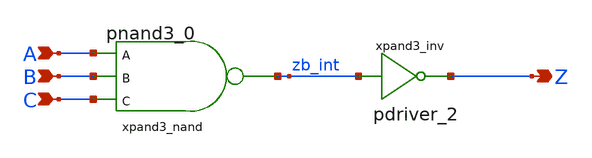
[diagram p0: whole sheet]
** sch_path: sram_2_16_scn4m/pand3.sch
**.subckt pand3 A B C Z
*.ipin A
*.ipin B
*.ipin C
*.opin Z
xpand3_nand A B C zb_int vdd gnd pnand3_0
xpand3_inv zb_int Z vdd gnd pdriver_2
**.ends
.end
